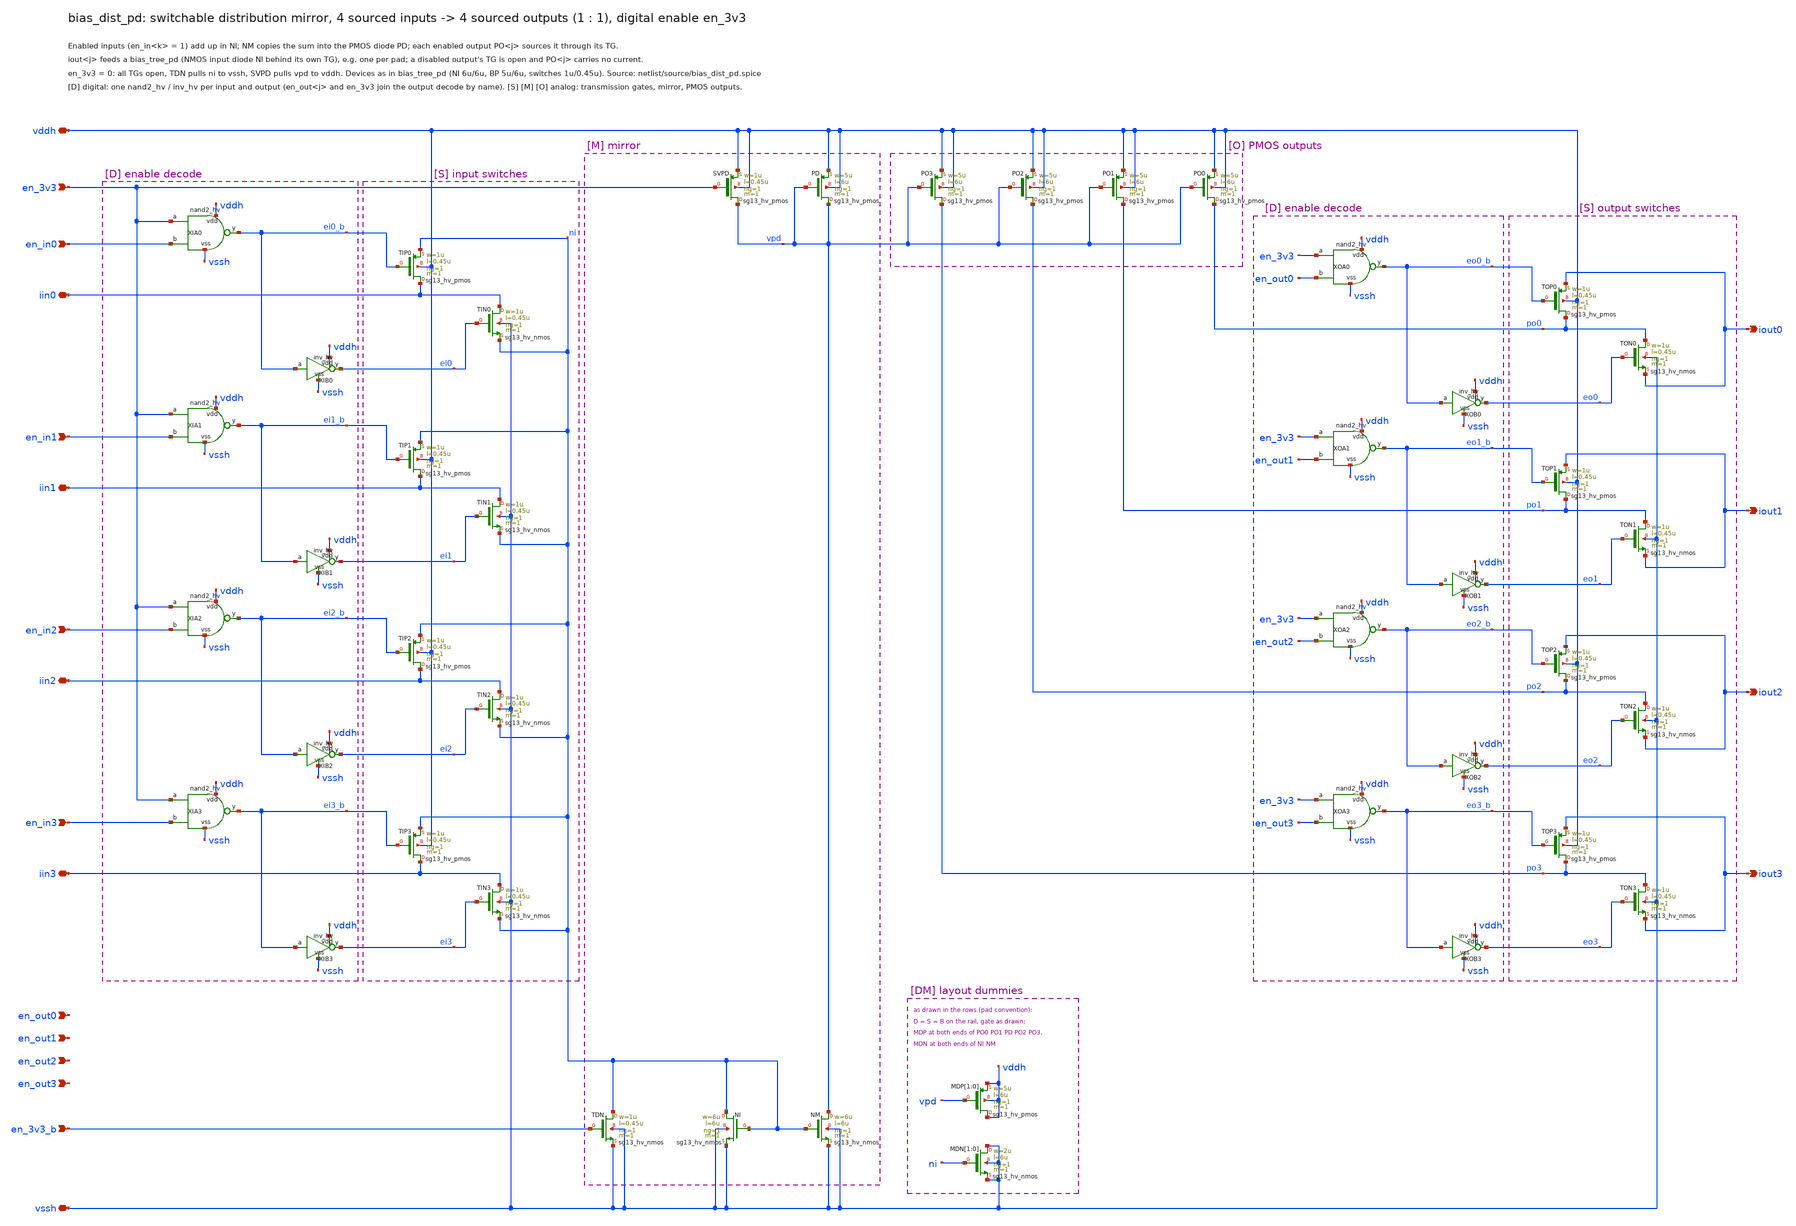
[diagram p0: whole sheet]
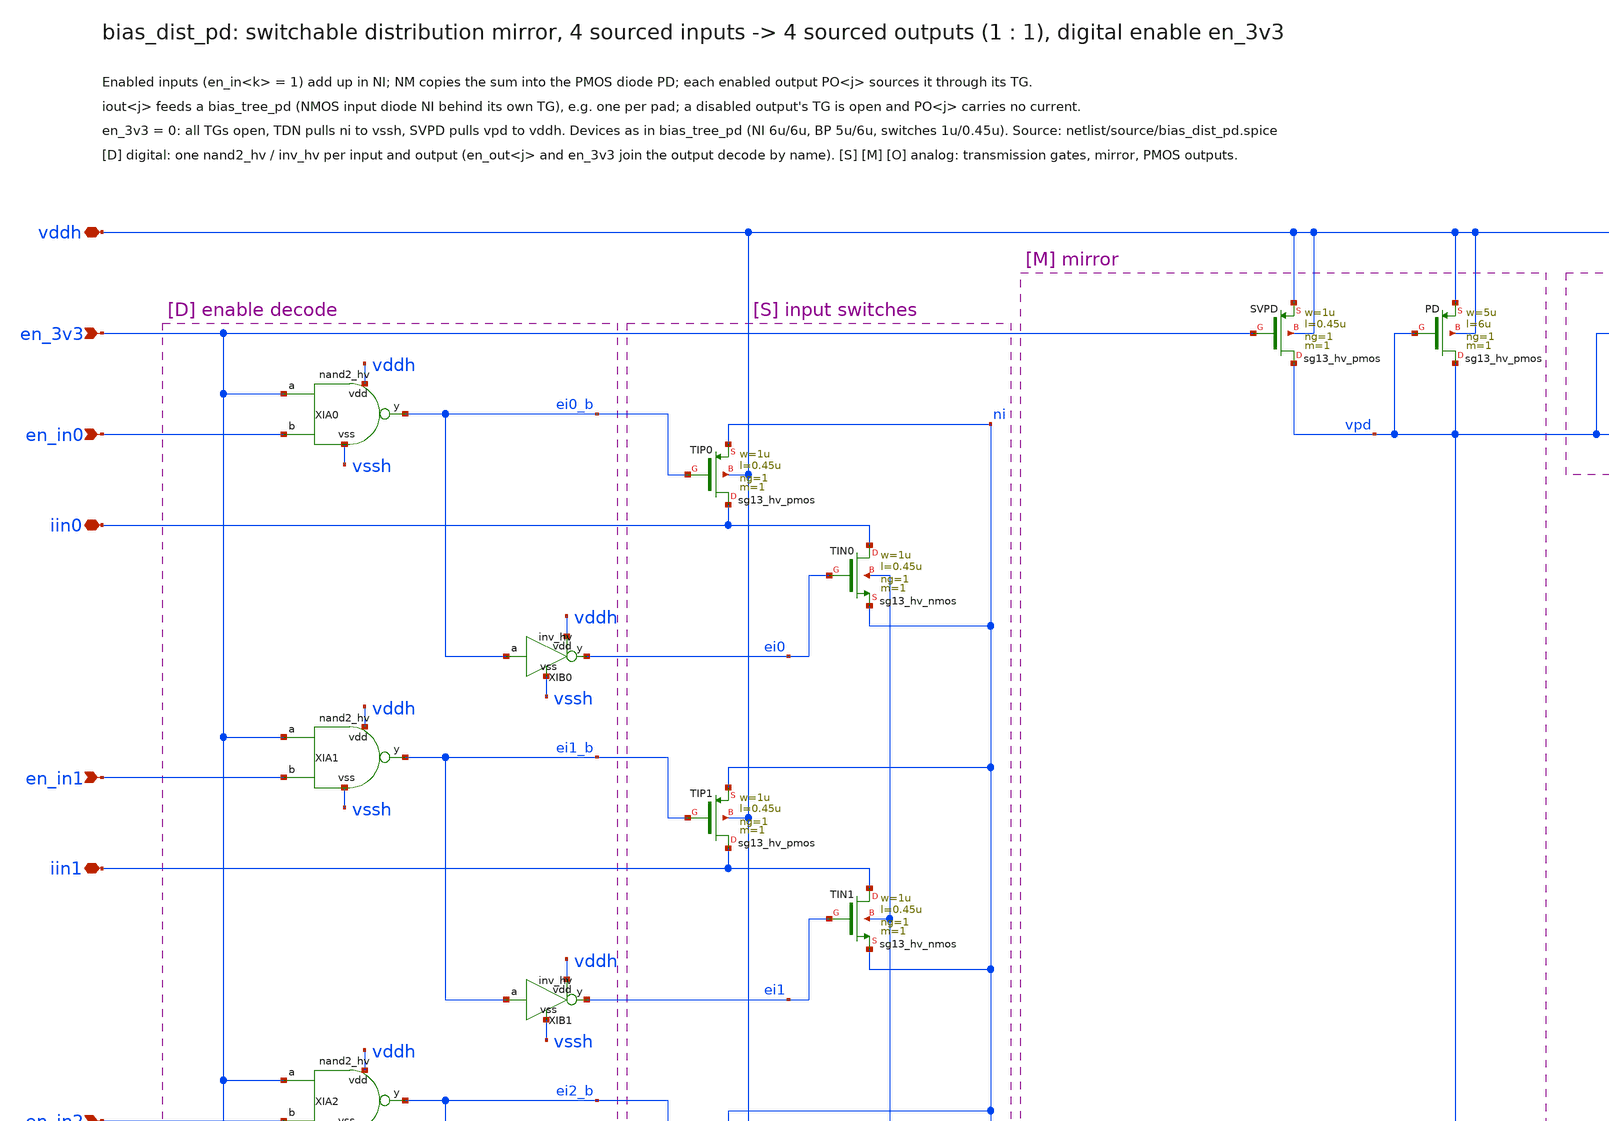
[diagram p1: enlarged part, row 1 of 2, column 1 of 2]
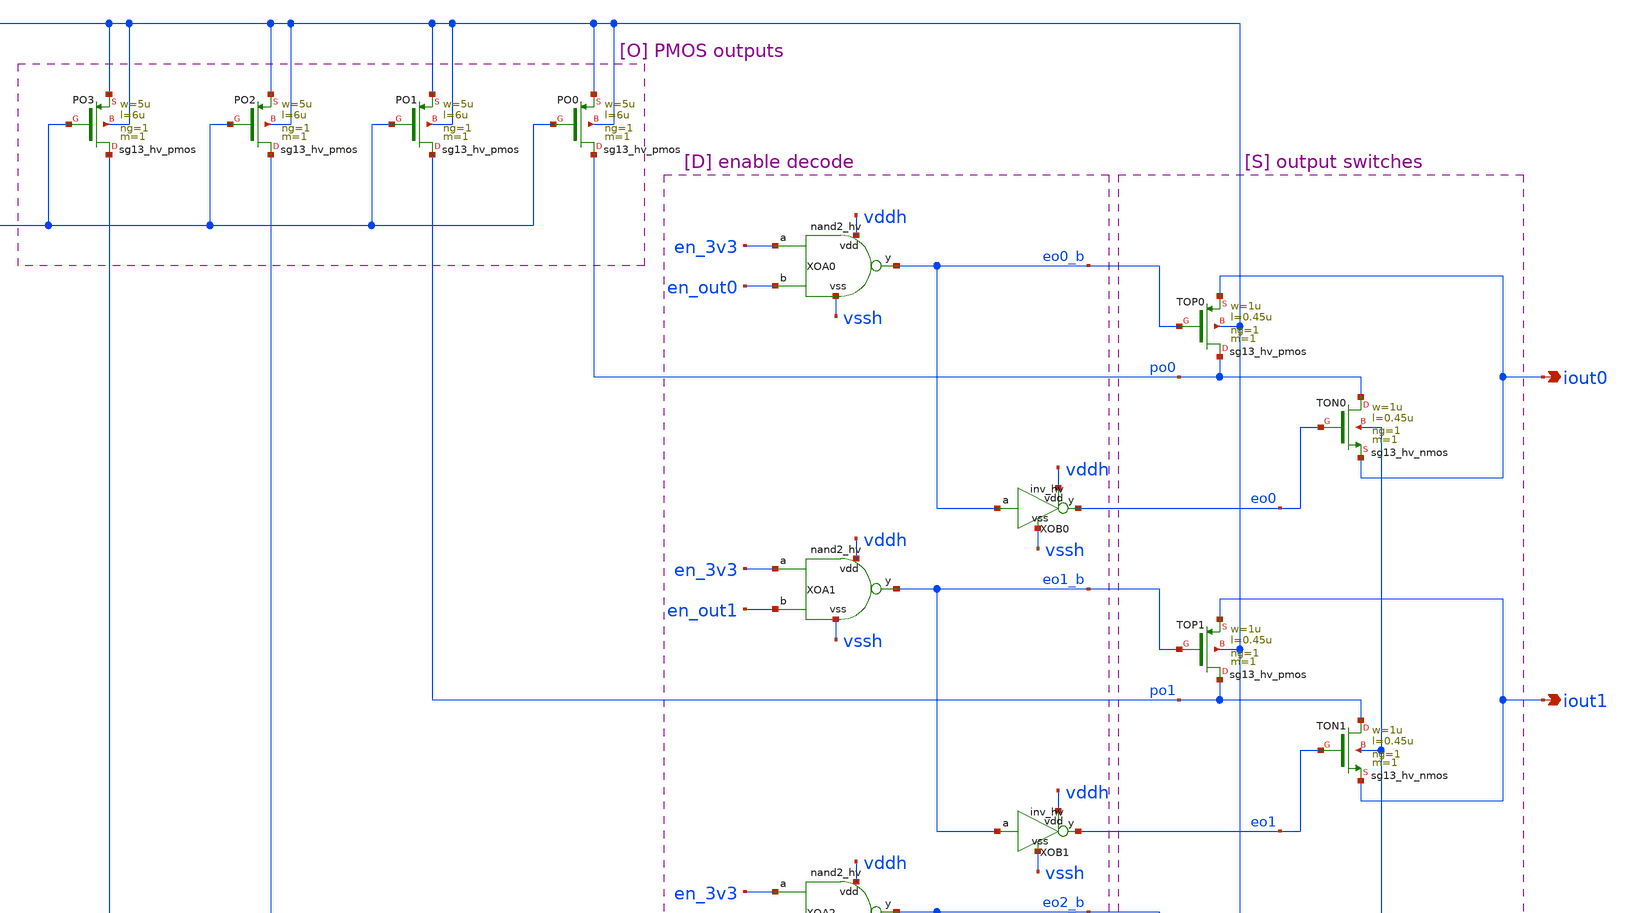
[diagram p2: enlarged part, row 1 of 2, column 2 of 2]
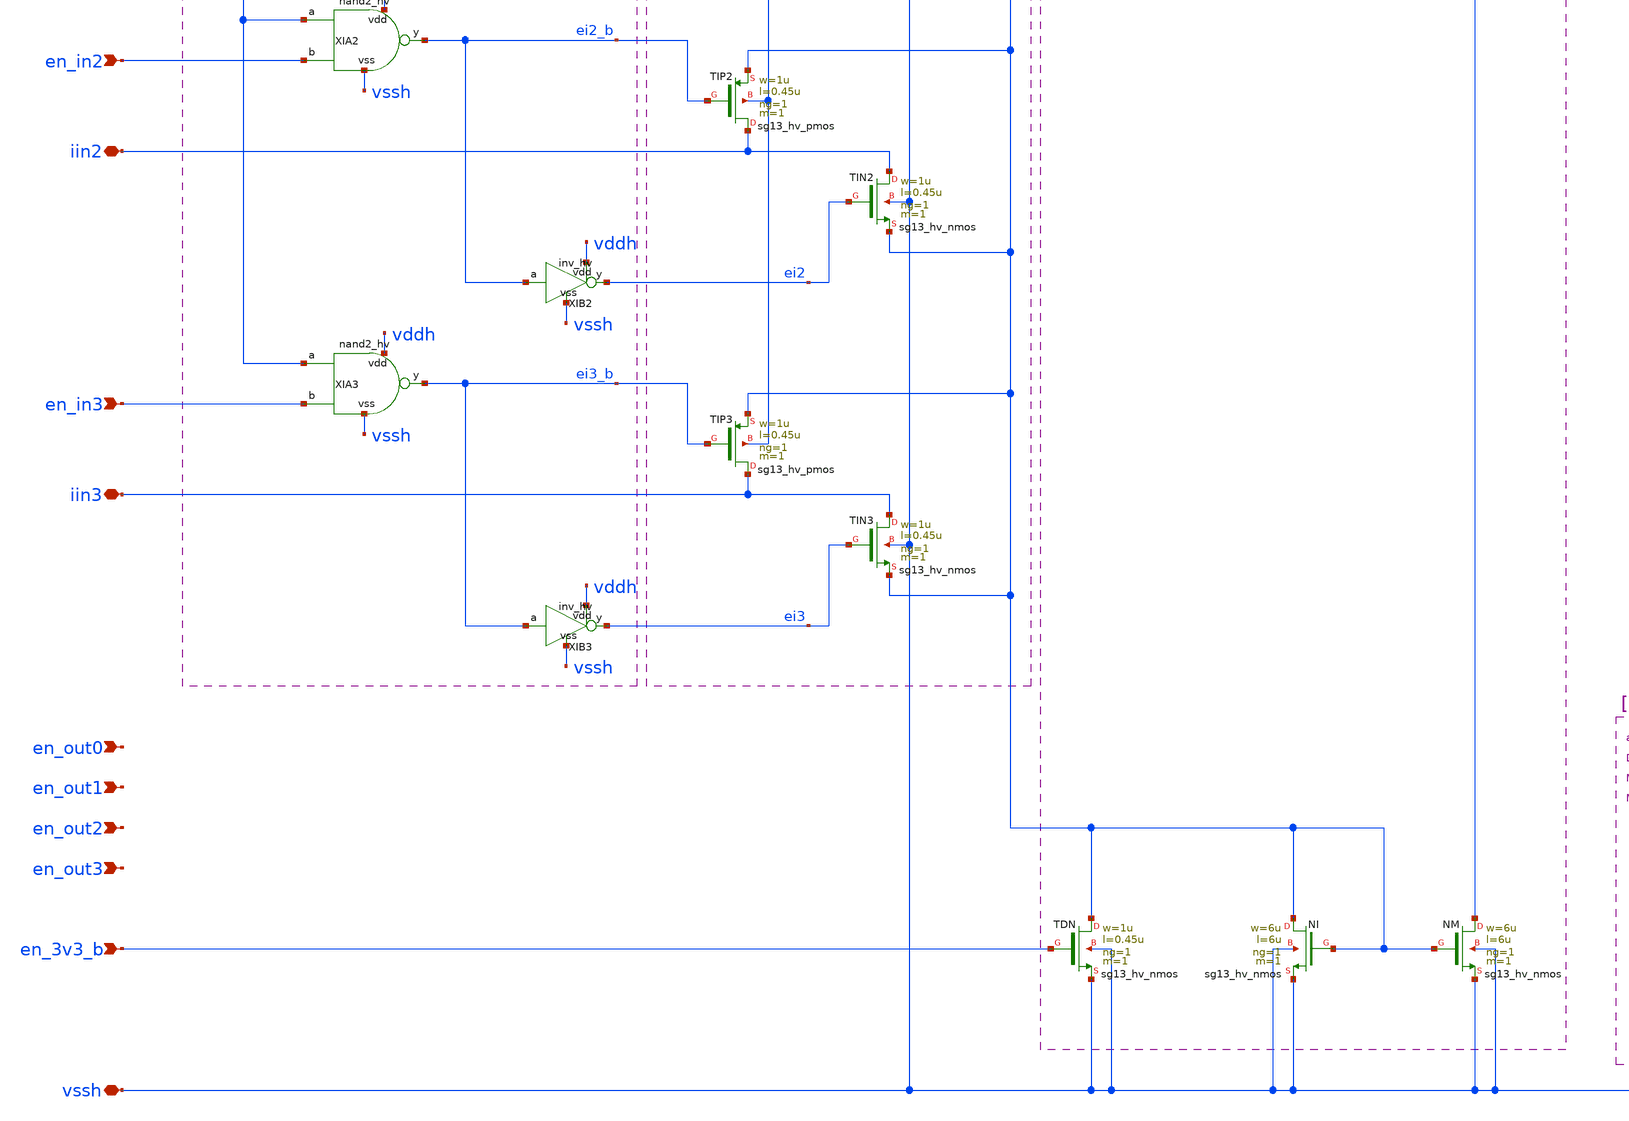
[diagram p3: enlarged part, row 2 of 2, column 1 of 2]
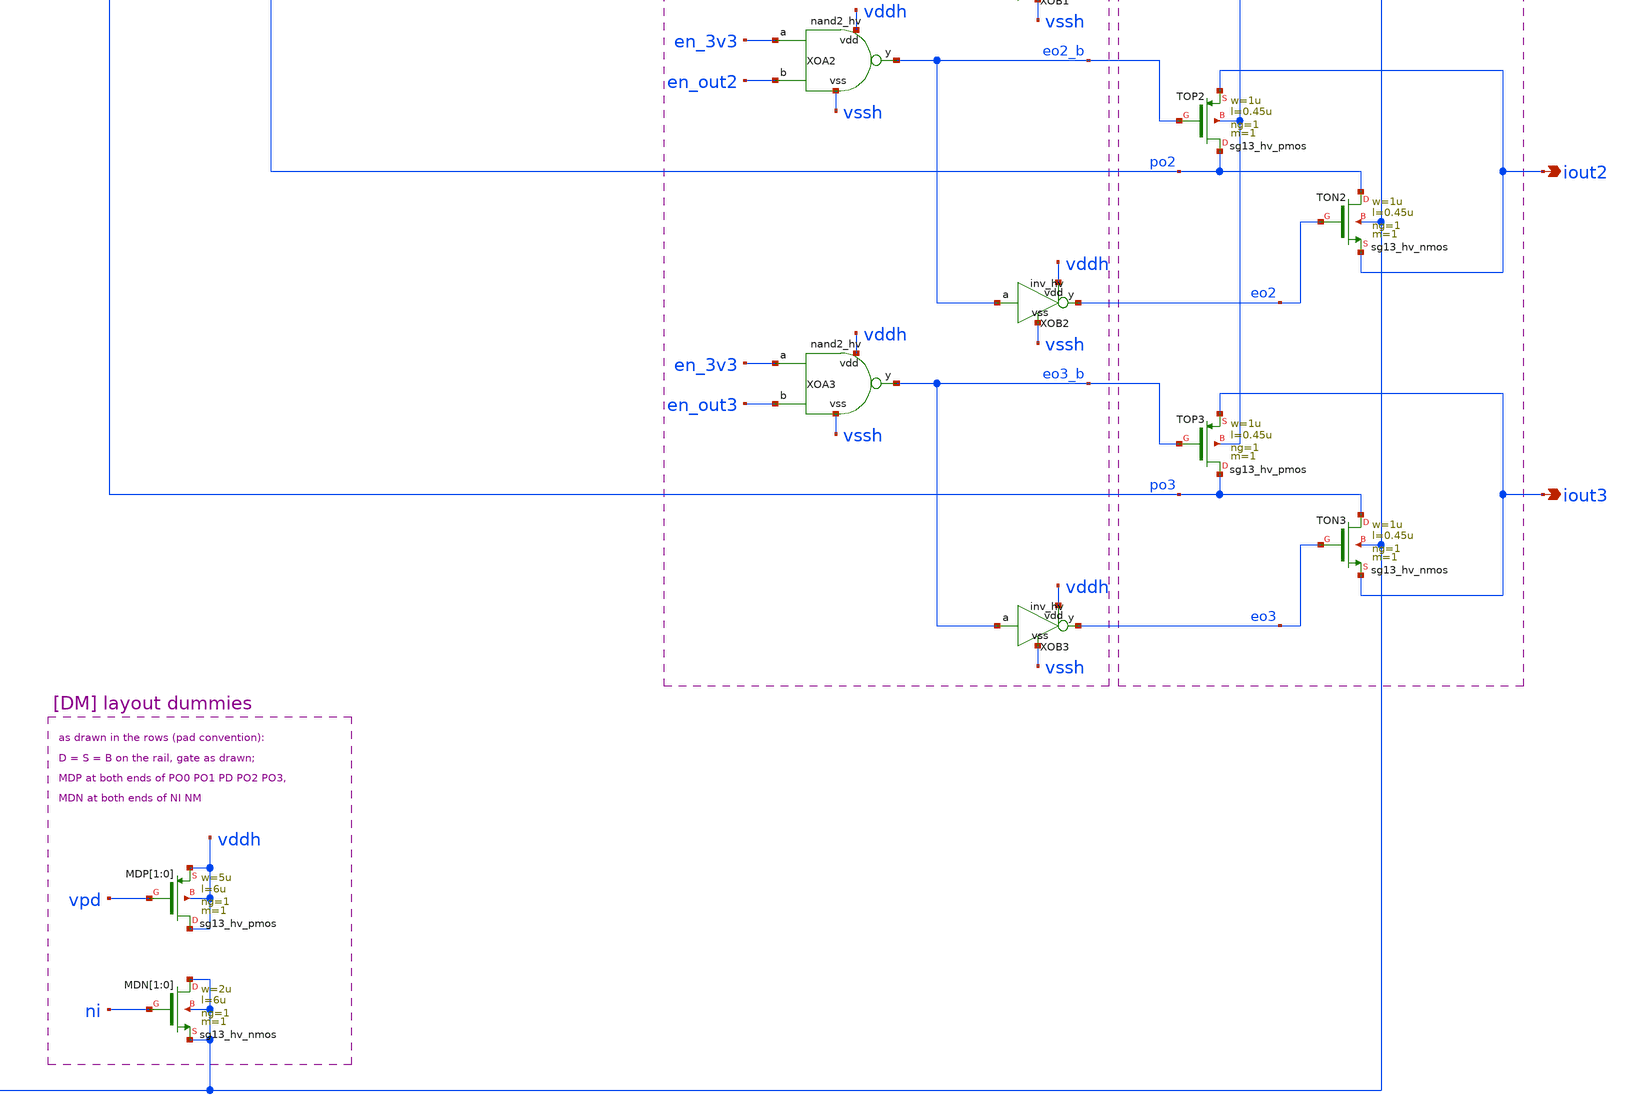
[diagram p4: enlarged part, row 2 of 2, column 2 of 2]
** sch_path: macros/bias_dist_pd/schematic/xschem/bias_dist_pd.sch
**.subckt bias_dist_pd vddh vssh en_3v3 en_3v3_b iin0 iin1 iin2 iin3 en_in0 en_in1 en_in2 en_in3
*+ iout0 iout1 iout2 iout3 en_out0 en_out1 en_out2 en_out3
*.iopin vddh
*.iopin vssh
*.ipin en_3v3
*.ipin en_3v3_b
*.iopin iin0
*.iopin iin1
*.iopin iin2
*.iopin iin3
*.ipin en_in0
*.ipin en_in1
*.ipin en_in2
*.ipin en_in3
*.opin iout0
*.opin iout1
*.opin iout2
*.opin iout3
*.ipin en_out0
*.ipin en_out1
*.ipin en_out2
*.ipin en_out3
XTIN0 iin0 ei0 ni vssh sg13_hv_nmos w=1u l=0.45u ng=1 m=1 mm_ok=1
XTIP0 iin0 ei0_b ni vddh sg13_hv_pmos w=1u l=0.45u ng=1 m=1 mm_ok=1
XTIN1 iin1 ei1 ni vssh sg13_hv_nmos w=1u l=0.45u ng=1 m=1 mm_ok=1
XTIP1 iin1 ei1_b ni vddh sg13_hv_pmos w=1u l=0.45u ng=1 m=1 mm_ok=1
XTIN2 iin2 ei2 ni vssh sg13_hv_nmos w=1u l=0.45u ng=1 m=1 mm_ok=1
XTIP2 iin2 ei2_b ni vddh sg13_hv_pmos w=1u l=0.45u ng=1 m=1 mm_ok=1
XTDN ni en_3v3_b vssh vssh sg13_hv_nmos w=1u l=0.45u ng=1 m=1 mm_ok=1
XNI ni ni vssh vssh sg13_hv_nmos w=6u l=6u ng=1 m=1 mm_ok=1
XNM vpd ni vssh vssh sg13_hv_nmos w=6u l=6u ng=1 m=1 mm_ok=1
XPD vpd vpd vddh vddh sg13_hv_pmos w=5u l=6u ng=1 m=1 mm_ok=1
XSVPD vpd en_3v3 vddh vddh sg13_hv_pmos w=1u l=0.45u ng=1 m=1 mm_ok=1
XPO0 po0 vpd vddh vddh sg13_hv_pmos w=5u l=6u ng=1 m=1 mm_ok=1
XTON0 po0 eo0 iout0 vssh sg13_hv_nmos w=1u l=0.45u ng=1 m=1 mm_ok=1
XTOP0 po0 eo0_b iout0 vddh sg13_hv_pmos w=1u l=0.45u ng=1 m=1 mm_ok=1
XPO1 po1 vpd vddh vddh sg13_hv_pmos w=5u l=6u ng=1 m=1 mm_ok=1
XTON1 po1 eo1 iout1 vssh sg13_hv_nmos w=1u l=0.45u ng=1 m=1 mm_ok=1
XTOP1 po1 eo1_b iout1 vddh sg13_hv_pmos w=1u l=0.45u ng=1 m=1 mm_ok=1
XPO2 po2 vpd vddh vddh sg13_hv_pmos w=5u l=6u ng=1 m=1 mm_ok=1
XTON2 po2 eo2 iout2 vssh sg13_hv_nmos w=1u l=0.45u ng=1 m=1 mm_ok=1
XTOP2 po2 eo2_b iout2 vddh sg13_hv_pmos w=1u l=0.45u ng=1 m=1 mm_ok=1
XPO3 po3 vpd vddh vddh sg13_hv_pmos w=5u l=6u ng=1 m=1 mm_ok=1
XTON3 po3 eo3 iout3 vssh sg13_hv_nmos w=1u l=0.45u ng=1 m=1 mm_ok=1
XTOP3 po3 eo3_b iout3 vddh sg13_hv_pmos w=1u l=0.45u ng=1 m=1 mm_ok=1
XIA0 vddh vssh en_3v3 en_in0 ei0_b nand2_hv
XIB0 vddh vssh ei0_b ei0 inv_hv
XIA1 vddh vssh en_3v3 en_in1 ei1_b nand2_hv
XIB1 vddh vssh ei1_b ei1 inv_hv
XIA2 vddh vssh en_3v3 en_in2 ei2_b nand2_hv
XIB2 vddh vssh ei2_b ei2 inv_hv
XOA0 vddh vssh en_3v3 en_out0 eo0_b nand2_hv
XOB0 vddh vssh eo0_b eo0 inv_hv
XOA1 vddh vssh en_3v3 en_out1 eo1_b nand2_hv
XOB1 vddh vssh eo1_b eo1 inv_hv
XOA2 vddh vssh en_3v3 en_out2 eo2_b nand2_hv
XOB2 vddh vssh eo2_b eo2 inv_hv
XOA3 vddh vssh en_3v3 en_out3 eo3_b nand2_hv
XOB3 vddh vssh eo3_b eo3 inv_hv
XTIN3 iin3 ei3 ni vssh sg13_hv_nmos w=1u l=0.45u ng=1 m=1 mm_ok=1
XTIP3 iin3 ei3_b ni vddh sg13_hv_pmos w=1u l=0.45u ng=1 m=1 mm_ok=1
XIA3 vddh vssh en_3v3 en_in3 ei3_b nand2_hv
XIB3 vddh vssh ei3_b ei3 inv_hv
XMDP[1] vddh vpd vddh vddh sg13_hv_pmos w=5u l=6u ng=1 m=1 mm_ok=1
XMDP[0] vddh vpd vddh vddh sg13_hv_pmos w=5u l=6u ng=1 m=1 mm_ok=1
XMDN[1] vssh ni vssh vssh sg13_hv_nmos w=2u l=6u ng=1 m=1 mm_ok=1
XMDN[0] vssh ni vssh vssh sg13_hv_nmos w=2u l=6u ng=1 m=1 mm_ok=1
**.ends

* expanding   symbol:  nand2_hv.sym # of pins=5
** sym_path: macros/hv_logic/schematic/xschem/nand2_hv.sym
** sch_path: macros/hv_logic/schematic/xschem/nand2_hv.sch
.subckt nand2_hv vdd vss a b y
*.iopin vdd
*.iopin vss
*.ipin a
*.ipin b
*.opin y
XPA y a vdd vdd sg13_hv_pmos w=1u l=0.45u ng=1 m=1 mm_ok=1
XPB y b vdd vdd sg13_hv_pmos w=1u l=0.45u ng=1 m=1 mm_ok=1
XNA y a n1 vss sg13_hv_nmos w=1u l=0.45u ng=1 m=1 mm_ok=1
XNB n1 b vss vss sg13_hv_nmos w=1u l=0.45u ng=1 m=1 mm_ok=1
.ends


* expanding   symbol:  inv_hv.sym # of pins=4
** sym_path: macros/hv_logic/schematic/xschem/inv_hv.sym
** sch_path: macros/hv_logic/schematic/xschem/inv_hv.sch
.subckt inv_hv vdd vss a y
*.iopin vdd
*.iopin vss
*.ipin a
*.opin y
XP y a vdd vdd sg13_hv_pmos w=1u l=0.45u ng=1 m=1 mm_ok=1
XN y a vss vss sg13_hv_nmos w=1u l=0.45u ng=1 m=1 mm_ok=1
.ends

.end
